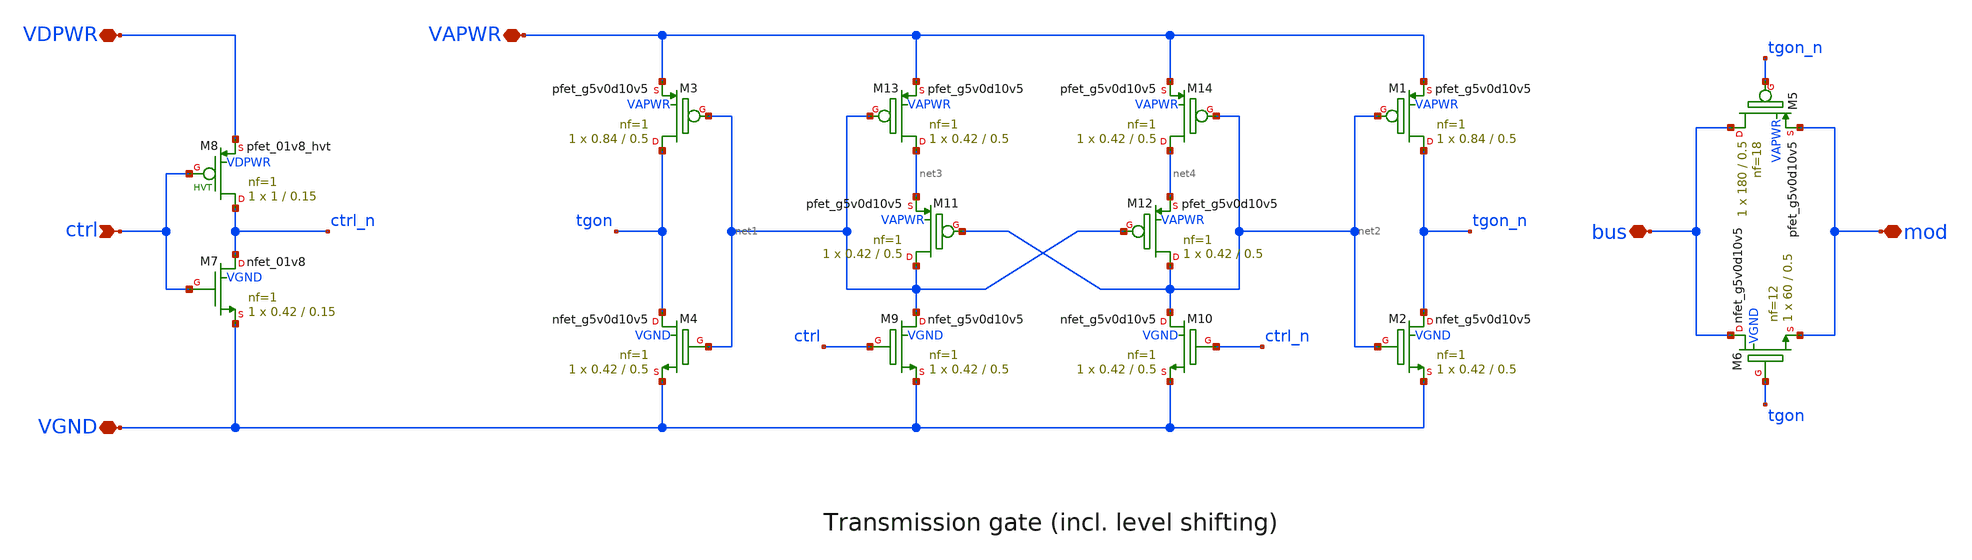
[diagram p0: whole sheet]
** sch_path: asw/sky130/tt_asw_3v3/xschem/tt_asw_3v3.sch
**.subckt tt_asw_3v3 mod bus ctrl VGND VDPWR VAPWR
*.iopin mod
*.iopin bus
*.ipin ctrl
*.iopin VGND
*.iopin VDPWR
*.iopin VAPWR
XM1 tgon_n net2 VAPWR VAPWR sky130_fd_pr__pfet_g5v0d10v5 L=0.5 W=0.84 nf=1 ad='int((nf+1)/2) * W/nf * 0.29'
+ as='int((nf+2)/2) * W/nf * 0.29' pd='2*int((nf+1)/2) * (W/nf + 0.29)' ps='2*int((nf+2)/2) * (W/nf + 0.29)'
+ nrd='0.29 / W' nrs='0.29 / W' sa=0 sb=0 sd=0 mult=1 m=1
XM2 tgon_n net2 VGND VGND sky130_fd_pr__nfet_g5v0d10v5 L=0.5 W=0.42 nf=1 ad='int((nf+1)/2) * W/nf * 0.29'
+ as='int((nf+2)/2) * W/nf * 0.29' pd='2*int((nf+1)/2) * (W/nf + 0.29)' ps='2*int((nf+2)/2) * (W/nf + 0.29)'
+ nrd='0.29 / W' nrs='0.29 / W' sa=0 sb=0 sd=0 mult=1 m=1
XM3 tgon net1 VAPWR VAPWR sky130_fd_pr__pfet_g5v0d10v5 L=0.5 W=0.84 nf=1 ad='int((nf+1)/2) * W/nf * 0.29'
+ as='int((nf+2)/2) * W/nf * 0.29' pd='2*int((nf+1)/2) * (W/nf + 0.29)' ps='2*int((nf+2)/2) * (W/nf + 0.29)'
+ nrd='0.29 / W' nrs='0.29 / W' sa=0 sb=0 sd=0 mult=1 m=1
XM4 tgon net1 VGND VGND sky130_fd_pr__nfet_g5v0d10v5 L=0.5 W=0.42 nf=1 ad='int((nf+1)/2) * W/nf * 0.29'
+ as='int((nf+2)/2) * W/nf * 0.29' pd='2*int((nf+1)/2) * (W/nf + 0.29)' ps='2*int((nf+2)/2) * (W/nf + 0.29)'
+ nrd='0.29 / W' nrs='0.29 / W' sa=0 sb=0 sd=0 mult=1 m=1
XM5 bus tgon_n mod VAPWR sky130_fd_pr__pfet_g5v0d10v5 L=0.5 W=180 nf=18 ad='int((nf+1)/2) * W/nf * 0.29'
+ as='int((nf+2)/2) * W/nf * 0.29' pd='2*int((nf+1)/2) * (W/nf + 0.29)' ps='2*int((nf+2)/2) * (W/nf + 0.29)'
+ nrd='0.29 / W' nrs='0.29 / W' sa=0 sb=0 sd=0 mult=1 m=1
XM6 bus tgon mod VGND sky130_fd_pr__nfet_g5v0d10v5 L=0.5 W=60 nf=12 ad='int((nf+1)/2) * W/nf * 0.29'
+ as='int((nf+2)/2) * W/nf * 0.29' pd='2*int((nf+1)/2) * (W/nf + 0.29)' ps='2*int((nf+2)/2) * (W/nf + 0.29)'
+ nrd='0.29 / W' nrs='0.29 / W' sa=0 sb=0 sd=0 mult=1 m=1
XM7 ctrl_n ctrl VGND VGND sky130_fd_pr__nfet_01v8 L=0.15 W=0.42 nf=1 ad='int((nf+1)/2) * W/nf * 0.29'
+ as='int((nf+2)/2) * W/nf * 0.29' pd='2*int((nf+1)/2) * (W/nf + 0.29)' ps='2*int((nf+2)/2) * (W/nf + 0.29)'
+ nrd='0.29 / W' nrs='0.29 / W' sa=0 sb=0 sd=0 mult=1 m=1
XM8 ctrl_n ctrl VDPWR VDPWR sky130_fd_pr__pfet_01v8_hvt L=0.15 W=1 nf=1 ad='int((nf+1)/2) * W/nf * 0.29'
+ as='int((nf+2)/2) * W/nf * 0.29' pd='2*int((nf+1)/2) * (W/nf + 0.29)' ps='2*int((nf+2)/2) * (W/nf + 0.29)'
+ nrd='0.29 / W' nrs='0.29 / W' sa=0 sb=0 sd=0 mult=1 m=1
XM9 net1 ctrl VGND VGND sky130_fd_pr__nfet_g5v0d10v5 L=0.5 W=0.42 nf=1 ad='int((nf+1)/2) * W/nf * 0.29'
+ as='int((nf+2)/2) * W/nf * 0.29' pd='2*int((nf+1)/2) * (W/nf + 0.29)' ps='2*int((nf+2)/2) * (W/nf + 0.29)'
+ nrd='0.29 / W' nrs='0.29 / W' sa=0 sb=0 sd=0 mult=1 m=1
XM10 net2 ctrl_n VGND VGND sky130_fd_pr__nfet_g5v0d10v5 L=0.5 W=0.42 nf=1 ad='int((nf+1)/2) * W/nf * 0.29'
+ as='int((nf+2)/2) * W/nf * 0.29' pd='2*int((nf+1)/2) * (W/nf + 0.29)' ps='2*int((nf+2)/2) * (W/nf + 0.29)'
+ nrd='0.29 / W' nrs='0.29 / W' sa=0 sb=0 sd=0 mult=1 m=1
XM11 net1 net2 net3 VAPWR sky130_fd_pr__pfet_g5v0d10v5 L=0.5 W=0.42 nf=1 ad='int((nf+1)/2) * W/nf * 0.29'
+ as='int((nf+2)/2) * W/nf * 0.29' pd='2*int((nf+1)/2) * (W/nf + 0.29)' ps='2*int((nf+2)/2) * (W/nf + 0.29)'
+ nrd='0.29 / W' nrs='0.29 / W' sa=0 sb=0 sd=0 mult=1 m=1
XM12 net2 net1 net4 VAPWR sky130_fd_pr__pfet_g5v0d10v5 L=0.5 W=0.42 nf=1 ad='int((nf+1)/2) * W/nf * 0.29'
+ as='int((nf+2)/2) * W/nf * 0.29' pd='2*int((nf+1)/2) * (W/nf + 0.29)' ps='2*int((nf+2)/2) * (W/nf + 0.29)'
+ nrd='0.29 / W' nrs='0.29 / W' sa=0 sb=0 sd=0 mult=1 m=1
XM13 net3 net1 VAPWR VAPWR sky130_fd_pr__pfet_g5v0d10v5 L=0.5 W=0.42 nf=1 ad='int((nf+1)/2) * W/nf * 0.29'
+ as='int((nf+2)/2) * W/nf * 0.29' pd='2*int((nf+1)/2) * (W/nf + 0.29)' ps='2*int((nf+2)/2) * (W/nf + 0.29)'
+ nrd='0.29 / W' nrs='0.29 / W' sa=0 sb=0 sd=0 mult=1 m=1
XM14 net4 net2 VAPWR VAPWR sky130_fd_pr__pfet_g5v0d10v5 L=0.5 W=0.42 nf=1 ad='int((nf+1)/2) * W/nf * 0.29'
+ as='int((nf+2)/2) * W/nf * 0.29' pd='2*int((nf+1)/2) * (W/nf + 0.29)' ps='2*int((nf+2)/2) * (W/nf + 0.29)'
+ nrd='0.29 / W' nrs='0.29 / W' sa=0 sb=0 sd=0 mult=1 m=1
**.ends
.end
